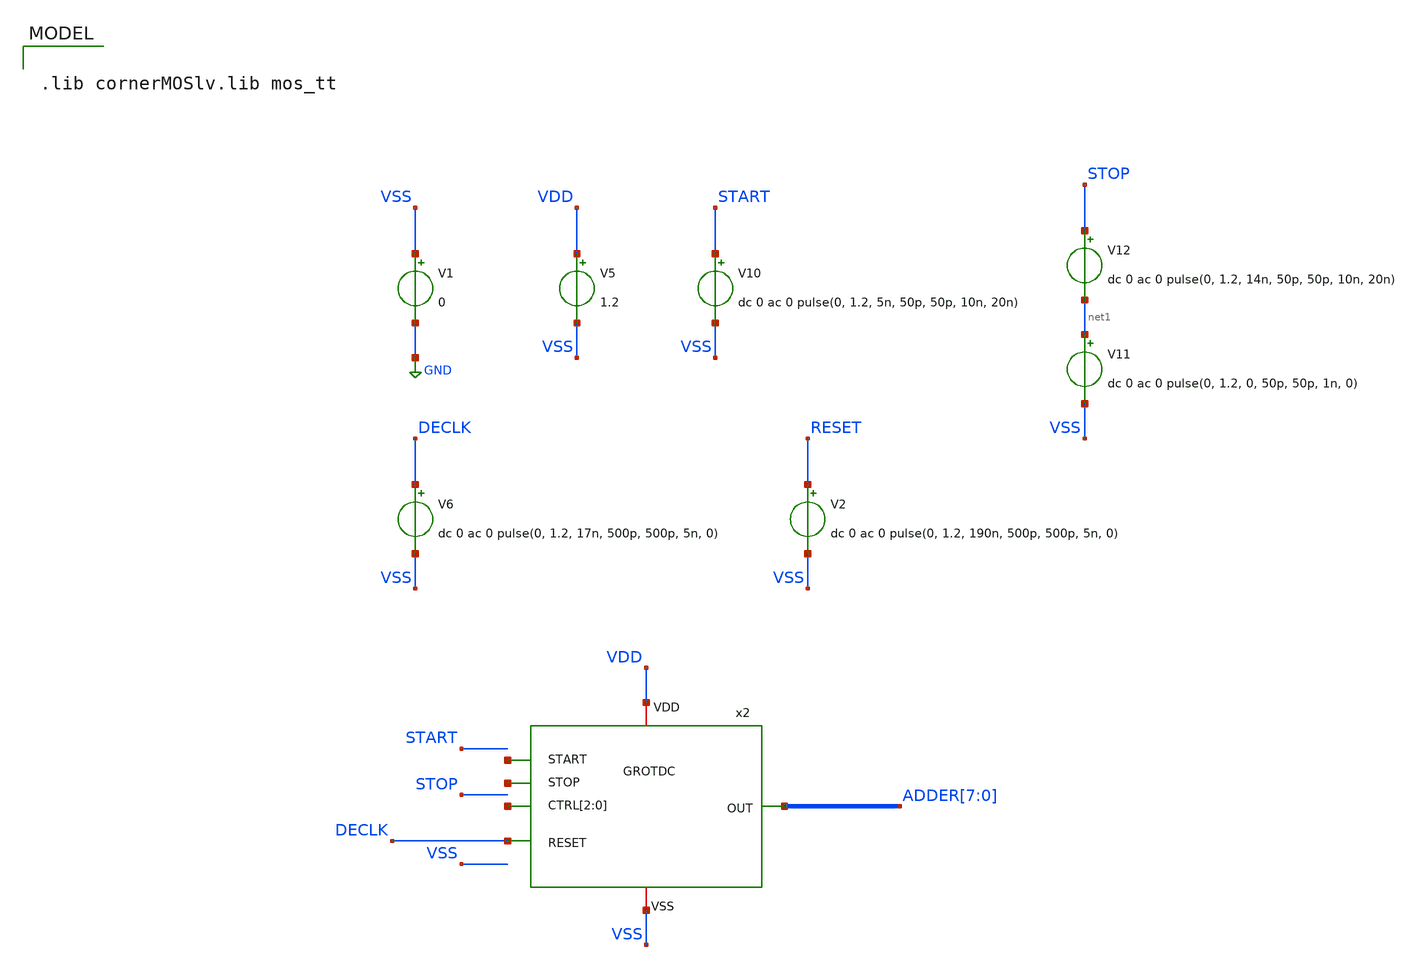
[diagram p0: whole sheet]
** sch_path: ADC8711-main/testbenches/tran/xschem/GROTDC_tb_v2.sch
**.subckt GROTDC_tb_v2
V1 VSS GND 0
V5 VDD VSS 1.2
V2 RESET VSS dc 0 ac 0 pulse(0, 1.2, 190n, 500p, 500p, 5n, 0)
V6 DECLK VSS dc 0 ac 0 pulse(0, 1.2, 17n, 500p, 500p, 5n, 0)
x2 ADDER[7] VDD net2 net3 VSS DECLK net4[2] net4[1] net4[0] GROTDC
V10 START VSS dc 0 ac 0 pulse(0, 1.2, 5n, 50p, 50p, 10n, 20n)
V11 net1 VSS dc 0 ac 0 pulse(0, 1.2, 0, 50p, 50p, 1n, 0)
V12 STOP net1 dc 0 ac 0 pulse(0, 1.2, 14n, 50p, 50p, 10n, 20n)
**** begin user architecture code

.lib cornerMOSlv.lib mos_tt



.param temp=65


.control
save all
tran 10p 50n
* Sources
let START = v(START)
let STOP = v(STOP)
let DECLK = v(DECLK)
let RESET = v(RESET)

* GRO
let IN0 = v(x2.IN0)
let IN1 = v(x2.IN1)
let IN2 = v(x2.IN2)

* Buffers
let K0 = v(x2.K0)
let K1 = v(x2.K1)
let K2 = v(x2.K2)

* Counters Reg
let D0_0 = v(x2.D0[0])
let D0_1 = v(x2.D0[1])
let D0_2 = v(x2.D0[2])
let D0_3 = v(x2.D0[3])
let D0_4 = v(x2.D0[4])
let D0_5 = v(x2.D0[5])
let D1_0 = v(x2.D1[0])
let D1_1 = v(x2.D1[1])
let D1_2 = v(x2.D1[2])
let D1_3 = v(x2.D1[3])
let D1_4 = v(x2.D1[4])
let D1_5 = v(x2.D1[5])
let D2_0 = v(x2.D2[0])
let D2_1 = v(x2.D2[1])
let D2_2 = v(x2.D2[2])
let D2_3 = v(x2.D2[3])
let D2_4 = v(x2.D2[4])
let D2_5 = v(x2.D2[5])

* FA
let S1_0 = v(x2.S1[0])
let S1_1 = v(x2.S1[1])
let S1_2 = v(x2.S1[2])
let S1_3 = v(x2.S1[3])
let S1_4 = v(x2.S1[4])
let S1_5 = v(x2.S1[5])
let COUT1 = v(x2.COUT1)
let S2_0 = v(x2.S2[0])
let S2_1 = v(x2.S2[1])
let S2_2 = v(x2.S2[2])
let S2_3 = v(x2.S2[3])
let S2_4 = v(x2.S2[4])
let S2_5 = v(x2.S2[5])
let S2_6 = v(x2.S2[6])
let COUT2 = v(x2.COUT2)

* FA Regs
let ADDER_0 = v(x2.ADDER[0])
let ADDER_1 = v(x2.ADDER[1])
let ADDER_2 = v(x2.ADDER[2])
let ADDER_3 = v(x2.ADDER[3])
let ADDER_4 = v(x2.ADDER[4])
let ADDER_5 = v(x2.ADDER[5])
let ADDER_6 = v(x2.ADDER[6])
let ADDER_7 = v(x2.ADDER[7])

write GROTDC_tb.raw
wrdata GRO_TDC_tb.raw time START STOP DECLK RESET IN0 IN1 IN2 K0 K1 K2 D0_0 D0_1 D0_2 D0_3 D0_4 D0_5
+ D1_0 D1_1 D1_2 D1_3 D1_4 D1_5 D2_0 D2_1 D2_2 D2_3 D2_4 D2_5 S1_0 S1_1 S1_2 S1_3 S1_4 S1_5 COUT1 S2_0
+ S2_1 S2_2 S2_3 S2_4 S2_5 S2_6 COUT2 ADDER_0 ADDER_1 ADDER_2 ADDER_3 ADDER_4 ADDER_5 ADDER_6  ADDER_7


*set appendwrite

.endc


**** end user architecture code
**.ends
.GLOBAL GND
.end
